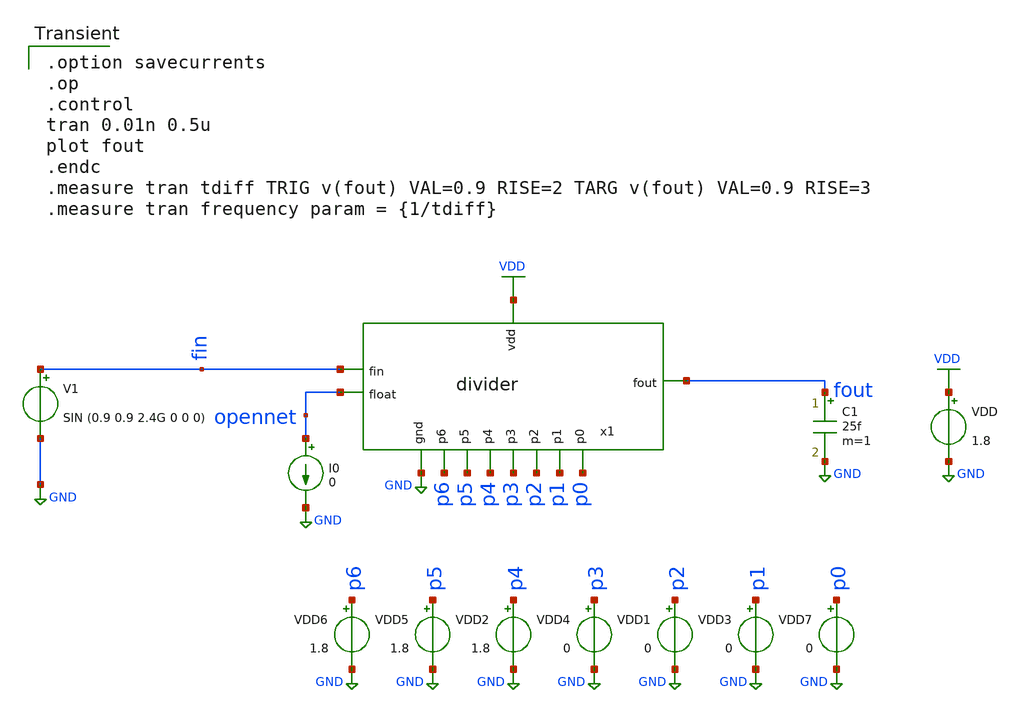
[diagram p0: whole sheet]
** sch_path: pll/dividers_lib/divider_design_trials/divider_2by3stages/divider_TB.sch
**.subckt divider_TB
VDD VDD GND 1.8
VDD1 p2 GND 0
VDD2 p4 GND 1.8
VDD3 p1 GND 0
VDD4 p3 GND 0
VDD5 p5 GND 1.8
VDD6 p6 GND 1.8
VDD7 p0 GND 0
V1 fin GND SIN (0.9 0.9 2.4G 0 0 0)
C1 fout GND 25f m=1
I0 opennet GND 0
x1 VDD fout fin opennet p0 p6 p5 p1 p2 p3 p4 GND divider
**** begin user architecture code

** opencircuitdesign pdks install
.lib $::SKYWATER_MODELS/sky130.lib.spice tt



.option savecurrents
.op
.control
tran 0.01n 0.5u
plot fout
.endc
.measure tran tdiff TRIG v(fout) VAL=0.9 RISE=2 TARG v(fout) VAL=0.9 RISE=3
.measure tran frequency param = {1/tdiff}

**** end user architecture code
**.ends
.GLOBAL VDD
.GLOBAL GND
.end
